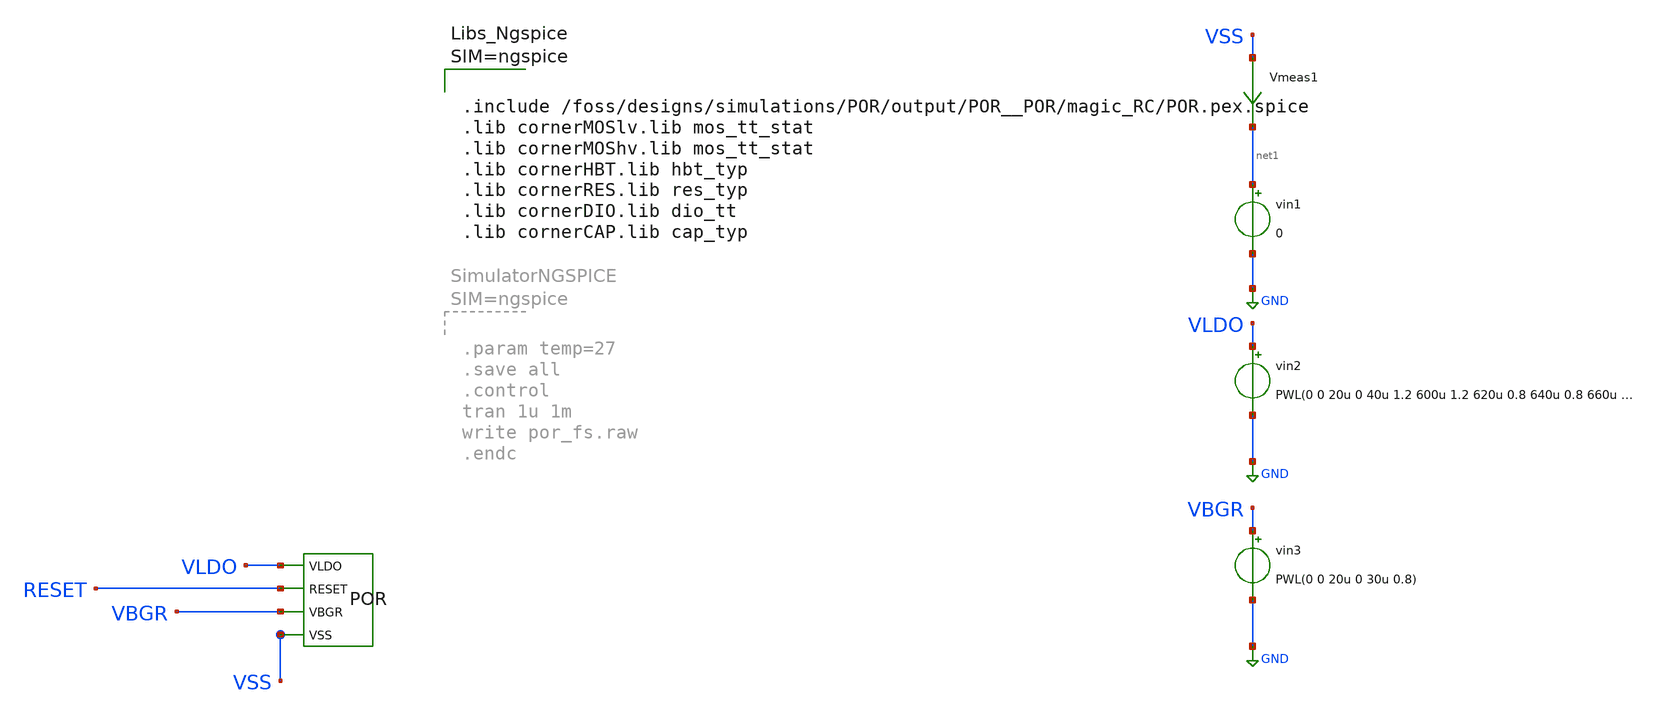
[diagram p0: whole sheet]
** sch_path: dependencies/POR/POR-main/testbenches/mc-tran/por_post_layout_sim_mc_mismatch.sch
**.subckt por_post_layout_sim_mc_mismatch
X1 VLDO RESET VBGR VSS POR
vin1 net1 GND 0
Vmeas1 VSS net1 0
.save i(vmeas1)
vin2 VLDO GND PWL(0 0 20u 0 40u 1.2 600u 1.2 620u 0.8 640u 0.8 660u 1.2 760u 1.2 780u 0)
vin3 VBGR GND PWL(0 0 20u 0 30u 0.8)
**** begin user architecture code



.include /foss/designs/simulations/POR/output/POR__POR/magic_RC/POR.pex.spice
.lib cornerMOSlv.lib mos_tt_stat
.lib cornerMOShv.lib mos_tt_stat
.lib cornerHBT.lib hbt_typ
.lib cornerRES.lib res_typ
.lib cornerDIO.lib dio_tt
.lib cornerCAP.lib cap_typ





.param mc_ok = 1
.param mm_ok = 1
.temp = -40 37 85

.control
save all
let mc_runs = 1000
let run = 0
set curplot=new
set scratch=$curplot
setplot $scratch

***************** LOOP *********************
dowhile run < mc_runs
save all
tran 1u 3m
set run=$&run
set ac=$curplot
setplot $scratch
let out{$run}={$ac}.reset
let time{$run}= {$ac}.time
setplot $ac
wrdata ../Power_on_reset/mc_stat/por_mc_stat{$&run}.csv {$ac}.reset
reset
let run=run+1
end
***************** LOOP *********************
plot {$scratch}.all vs {$scratch}.time0
write por_mc_stat.raw

.endc


**** end user architecture code
**.ends
.GLOBAL GND
.end
